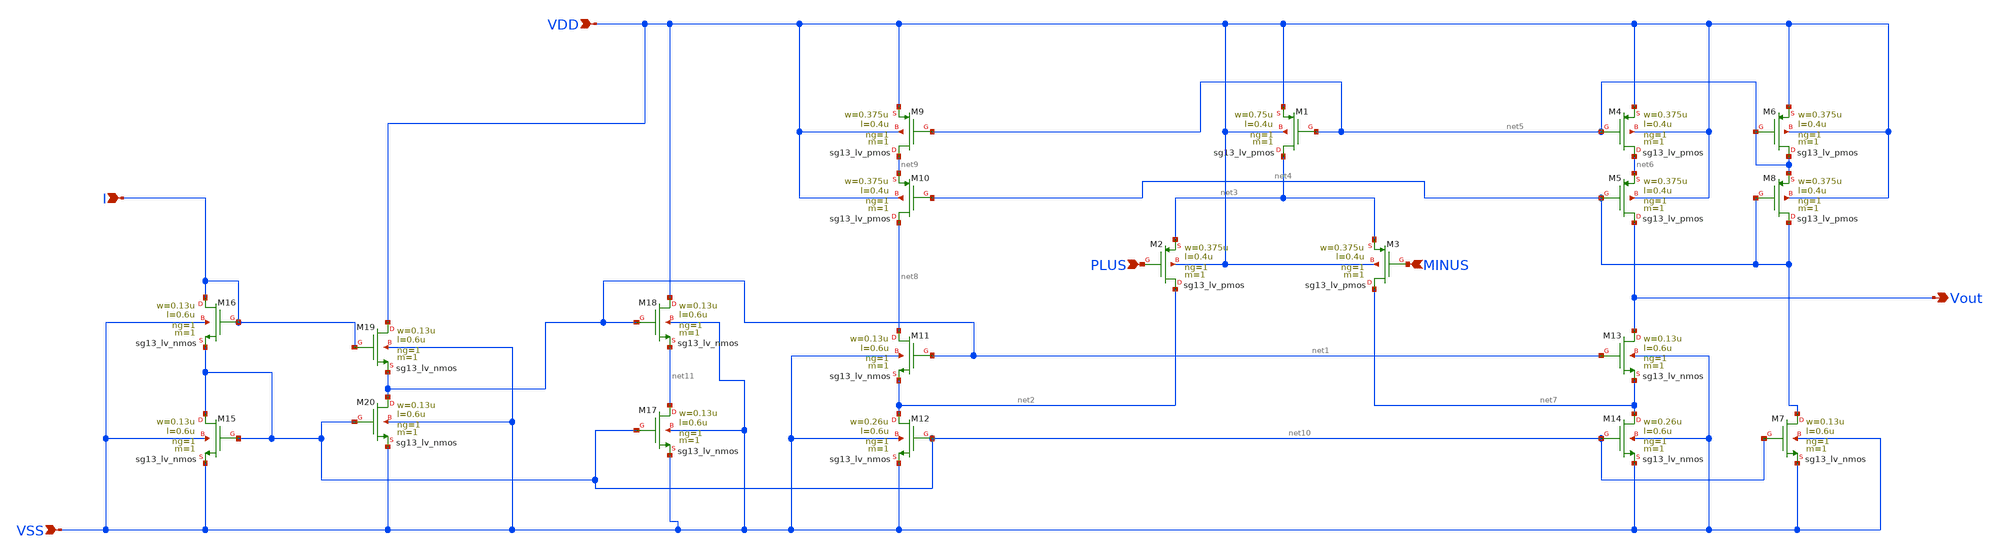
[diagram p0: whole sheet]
** sch_path: DSM/Schematics/RealCircuits/Folded Cascode/FoldCas_still_working_on_it.sch
* (c) 2024 Hrishikesh, @HSB
**.subckt FoldCas_still_working_on_it PLUS MINUS Vout VDD VSS I
*.ipin PLUS
*.ipin MINUS
*.opin Vout
*.ipin VDD
*.ipin VSS
*.ipin I
XM1 net3 net5 VDD VDD sg13_lv_pmos w=0.75u l=0.4u ng=1 m=1 mm_ok=1
XM2 net2 PLUS net3 VDD sg13_lv_pmos w=0.375u l=0.4u ng=1 m=1 mm_ok=1
XM3 net7 MINUS net3 VDD sg13_lv_pmos w=0.375u l=0.4u ng=1 m=1 mm_ok=1
XM14 net7 net10 VSS VSS sg13_lv_nmos w=0.26u l=0.6u ng=1 m=1 mm_ok=1
XM13 Vout net1 net7 VSS sg13_lv_nmos w=0.13u l=0.6u ng=1 m=1 mm_ok=1
XM11 net8 net1 net2 VSS sg13_lv_nmos w=0.13u l=0.6u ng=1 m=1 mm_ok=1
XM12 net2 net10 VSS VSS sg13_lv_nmos w=0.26u l=0.6u ng=1 m=1 mm_ok=1
XM9 net9 net5 VDD VDD sg13_lv_pmos w=0.375u l=0.4u ng=1 m=1 mm_ok=1
XM10 net8 net4 net9 VDD sg13_lv_pmos w=0.375u l=0.4u ng=1 m=1 mm_ok=1
XM4 net6 net5 VDD VDD sg13_lv_pmos w=0.375u l=0.4u ng=1 m=1 mm_ok=1
XM5 Vout net4 net6 VDD sg13_lv_pmos w=0.375u l=0.4u ng=1 m=1 mm_ok=1
XM6 net5 net5 VDD VDD sg13_lv_pmos w=0.375u l=0.4u ng=1 m=1 mm_ok=1
XM8 net4 net4 net5 VDD sg13_lv_pmos w=0.375u l=0.4u ng=1 m=1 mm_ok=1
XM7 net4 net10 VSS VSS sg13_lv_nmos w=0.13u l=0.6u ng=1 m=1 mm_ok=1
XM18 VDD net1 net11 VSS sg13_lv_nmos w=0.13u l=0.6u ng=1 m=1 mm_ok=1
XM17 net11 net10 VSS VSS sg13_lv_nmos w=0.13u l=0.6u ng=1 m=1 mm_ok=1
XM19 VDD I net1 VSS sg13_lv_nmos w=0.13u l=0.6u ng=1 m=1 mm_ok=1
XM20 net1 net10 VSS VSS sg13_lv_nmos w=0.13u l=0.6u ng=1 m=1 mm_ok=1
XM16 I I net10 VSS sg13_lv_nmos w=0.13u l=0.6u ng=1 m=1 mm_ok=1
XM15 net10 net10 VSS VSS sg13_lv_nmos w=0.13u l=0.6u ng=1 m=1 mm_ok=1
**.ends
.end
